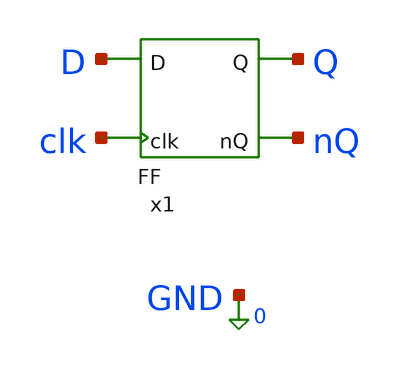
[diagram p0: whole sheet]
** sch_path: xschem_designs/FF_TB.sch
**.subckt FF_TB
x1 D Q nQ clk FF
**** begin user architecture code


.global VDD GND BP BN
.option temp=27
.include /usr/local/share/pdk/gf180mcuC/libs.tech/ngspice/design.ngspice
.lib /usr/local/share/pdk/gf180mcuC/libs.tech/ngspice/sm141064.ngspice typical

Vdd VDD 0 3.3
Vbp BP VDD 2.7
Vbn BN GND -2.7
Va a 0 PWL(0 0 89.9n 0 90.1n 1.4 179.9n 1.4 180.1n 3.3 270n 3.3)
Vb b 0 PWL(0 0 29.9n 0 30.1n 1.4 59.9n 1.4 60.1n 3.3 89.9n 3.3 90.1n 0 119.9n 0 120.1n 1.4 149.9n
+ 1.4 150.1n 3.3 179.9n 3.3 180.1n 0 209.9n 0 210.1n 1.4 239.9n 1.4 240.1n 3.3 270n 3.3)
VD D 0 PWL(0n 0 14.9n 0 15.1n 1.4 74.9n 1.4 75.1n 3.3 134.9n 3.3 135.1n 1.4 194.9n 1.4 195.1n 0
+ 254.9n 0 255.1n 3.3 314.9n 3.3 315.1n 0 374.9n 0 375.1n 0 434.9ns 0 435.1n 1.4 494.9n 1.4 495.1n 1.4
+ 554.9n 1.4 555.1n 3.3 615n 3.3)
Vclk clk 0 PULSE(3.3 0 29.9n 0.2n 0.2n 29.8n 60n)

.control
  save all
  tran 0.05n 615n
  write FF_TB.raw
.endc
.end


**** end user architecture code
**.ends

* expanding   symbol:  xschem_designs/FF.sym # of pins=4
** sym_path: xschem_designs/FF.sym
** sch_path: xschem_designs/FF.sch
.subckt FF D Q nQ clk
*.ipin clk
*.ipin D
*.opin Q
*.opin nQ
x2 net3 clk D NMIN
x4 net4 net5 clk NMIN
x5 net1 net3 net2 NMIN
x6 net2 net1 net4 NMIN
x7 net6 net8 net1 NMIN
x8 net7 net2 net8 NMIN
x9 Q net6 nQ NMIN
x10 nQ Q net7 NMIN
XM21 net8 clk VDD VDD pfet_03v3 L=0.28u W=0.44u nf=1 ad='int((nf+1)/2) * W/nf * 0.18u' as='int((nf+2)/2) * W/nf * 0.18u'
+ pd='2*int((nf+1)/2) * (W/nf + 0.18u)' ps='2*int((nf+2)/2) * (W/nf + 0.18u)' nrd='0.18u / W' nrs='0.18u / W'
+ sa=0 sb=0 sd=0 m=1 par=1
XM29 net8 clk GND GND nfet_03v3 L=0.28u W=0.22u nf=1 ad='int((nf+1)/2) * W/nf * 0.18u' as='int((nf+2)/2) * W/nf * 0.18u'
+ pd='2*int((nf+1)/2) * (W/nf + 0.18u)' ps='2*int((nf+2)/2) * (W/nf + 0.18u)' nrd='0.18u / W' nrs='0.18u / W'
+ sa=0 sb=0 sd=0 m=1 par=1
x1 net5 D STI
.ends


* expanding   symbol:  xschem_designs/NMIN.sym # of pins=3
** sym_path: xschem_designs/NMIN.sym
** sch_path: xschem_designs/NMIN.sch
.subckt NMIN out a b
*.ipin a
*.ipin b
*.opin out
XM21 net1 a VDD VDD pfet_03v3 L=0.28u W=0.44u nf=1 ad='int((nf+1)/2) * W/nf * 0.18u' as='int((nf+2)/2) * W/nf * 0.18u'
+ pd='2*int((nf+1)/2) * (W/nf + 0.18u)' ps='2*int((nf+2)/2) * (W/nf + 0.18u)' nrd='0.18u / W' nrs='0.18u / W'
+ sa=0 sb=0 sd=0 m=1 par=1
XM22 out out net1 VDD pfet_03v3 L=1.12u W=0.22u nf=1 ad='int((nf+1)/2) * W/nf * 0.18u' as='int((nf+2)/2) * W/nf * 0.18u'
+ pd='2*int((nf+1)/2) * (W/nf + 0.18u)' ps='2*int((nf+2)/2) * (W/nf + 0.18u)' nrd='0.18u / W' nrs='0.18u / W'
+ sa=0 sb=0 sd=0 m=1 par=1
XM23 out a VDD BP pfet_06v0 L=1.1u W=0.60u nf=1 ad='int((nf+1)/2) * W/nf * 0.18u' as='int((nf+2)/2) * W/nf * 0.18u'
+ pd='2*int((nf+1)/2) * (W/nf + 0.18u)' ps='2*int((nf+2)/2) * (W/nf + 0.18u)' nrd='0.18u / W' nrs='0.18u / W'
+ sa=0 sb=0 sd=0 m=1 par=1
XM24 out b VDD BP pfet_06v0 L=1.1u W=0.60u nf=1 ad='int((nf+1)/2) * W/nf * 0.18u' as='int((nf+2)/2) * W/nf * 0.18u'
+ pd='2*int((nf+1)/2) * (W/nf + 0.18u)' ps='2*int((nf+2)/2) * (W/nf + 0.18u)' nrd='0.18u / W' nrs='0.18u / W'
+ sa=0 sb=0 sd=0 m=1 par=1
XM25 net1 b VDD VDD pfet_03v3 L=0.28u W=0.44u nf=1 ad='int((nf+1)/2) * W/nf * 0.18u' as='int((nf+2)/2) * W/nf * 0.18u'
+ pd='2*int((nf+1)/2) * (W/nf + 0.18u)' ps='2*int((nf+2)/2) * (W/nf + 0.18u)' nrd='0.18u / W' nrs='0.18u / W'
+ sa=0 sb=0 sd=0 m=1 par=1
XM26 out out net2 GND nfet_03v3 L=2.24u W=0.22u nf=1 ad='int((nf+1)/2) * W/nf * 0.18u' as='int((nf+2)/2) * W/nf * 0.18u'
+ pd='2*int((nf+1)/2) * (W/nf + 0.18u)' ps='2*int((nf+2)/2) * (W/nf + 0.18u)' nrd='0.18u / W' nrs='0.18u / W'
+ sa=0 sb=0 sd=0 m=1 par=1
XM27 net3 a GND BN nfet_06v0 L=1.4u W=0.30u nf=1 ad='int((nf+1)/2) * W/nf * 0.18u' as='int((nf+2)/2) * W/nf * 0.18u'
+ pd='2*int((nf+1)/2) * (W/nf + 0.18u)' ps='2*int((nf+2)/2) * (W/nf + 0.18u)' nrd='0.18u / W' nrs='0.18u / W'
+ sa=0 sb=0 sd=0 m=1 par=1
XM28 out b net3 BN nfet_06v0 L=1.4u W=0.30u nf=1 ad='int((nf+1)/2) * W/nf * 0.18u' as='int((nf+2)/2) * W/nf * 0.18u'
+ pd='2*int((nf+1)/2) * (W/nf + 0.18u)' ps='2*int((nf+2)/2) * (W/nf + 0.18u)' nrd='0.18u / W' nrs='0.18u / W'
+ sa=0 sb=0 sd=0 m=1 par=1
XM29 net4 a GND GND nfet_03v3 L=0.28u W=0.22u nf=1 ad='int((nf+1)/2) * W/nf * 0.18u' as='int((nf+2)/2) * W/nf * 0.18u'
+ pd='2*int((nf+1)/2) * (W/nf + 0.18u)' ps='2*int((nf+2)/2) * (W/nf + 0.18u)' nrd='0.18u / W' nrs='0.18u / W'
+ sa=0 sb=0 sd=0 m=1 par=1
XM30 net2 b net4 GND nfet_03v3 L=0.28u W=0.22u nf=1 ad='int((nf+1)/2) * W/nf * 0.18u' as='int((nf+2)/2) * W/nf * 0.18u'
+ pd='2*int((nf+1)/2) * (W/nf + 0.18u)' ps='2*int((nf+2)/2) * (W/nf + 0.18u)' nrd='0.18u / W' nrs='0.18u / W'
+ sa=0 sb=0 sd=0 m=1 par=1
.ends


* expanding   symbol:  xschem_designs/STI.sym # of pins=2
** sym_path: xschem_designs/STI.sym
** sch_path: xschem_designs/STI.sch
.subckt STI out in
*.ipin in
*.opin out
XM225 out out net1 GND nfet_03v3 L=2.24u W=0.22u nf=1 ad='int((nf+1)/2) * W/nf * 0.18u' as='int((nf+2)/2) * W/nf * 0.18u'
+ pd='2*int((nf+1)/2) * (W/nf + 0.18u)' ps='2*int((nf+2)/2) * (W/nf + 0.18u)' nrd='0.18u / W' nrs='0.18u / W'
+ sa=0 sb=0 sd=0 m=1 par=1
XM226 out out net2 VDD pfet_03v3 L=1.12u W=0.22u nf=1 ad='int((nf+1)/2) * W/nf * 0.18u' as='int((nf+2)/2) * W/nf * 0.18u'
+ pd='2*int((nf+1)/2) * (W/nf + 0.18u)' ps='2*int((nf+2)/2) * (W/nf + 0.18u)' nrd='0.18u / W' nrs='0.18u / W'
+ sa=0 sb=0 sd=0 m=1 par=1
XM237 net2 in VDD VDD pfet_03v3 L=0.28u W=0.44u nf=1 ad='int((nf+1)/2) * W/nf * 0.18u' as='int((nf+2)/2) * W/nf * 0.18u'
+ pd='2*int((nf+1)/2) * (W/nf + 0.18u)' ps='2*int((nf+2)/2) * (W/nf + 0.18u)' nrd='0.18u / W' nrs='0.18u / W'
+ sa=0 sb=0 sd=0 m=1 par=1
XM238 net1 in GND GND nfet_03v3 L=0.28u W=0.22u nf=1 ad='int((nf+1)/2) * W/nf * 0.18u' as='int((nf+2)/2) * W/nf * 0.18u'
+ pd='2*int((nf+1)/2) * (W/nf + 0.18u)' ps='2*int((nf+2)/2) * (W/nf + 0.18u)' nrd='0.18u / W' nrs='0.18u / W'
+ sa=0 sb=0 sd=0 m=1 par=1
XM241 out in VDD BP pfet_06v0 L=1.1u W=0.60u nf=1 ad='int((nf+1)/2) * W/nf * 0.18u' as='int((nf+2)/2) * W/nf * 0.18u'
+ pd='2*int((nf+1)/2) * (W/nf + 0.18u)' ps='2*int((nf+2)/2) * (W/nf + 0.18u)' nrd='0.18u / W' nrs='0.18u / W'
+ sa=0 sb=0 sd=0 m=1 par=1
XM242 out in GND BN nfet_06v0 L=1.4u W=0.30u nf=1 ad='int((nf+1)/2) * W/nf * 0.18u' as='int((nf+2)/2) * W/nf * 0.18u'
+ pd='2*int((nf+1)/2) * (W/nf + 0.18u)' ps='2*int((nf+2)/2) * (W/nf + 0.18u)' nrd='0.18u / W' nrs='0.18u / W'
+ sa=0 sb=0 sd=0 m=1 par=1
.ends

.end
